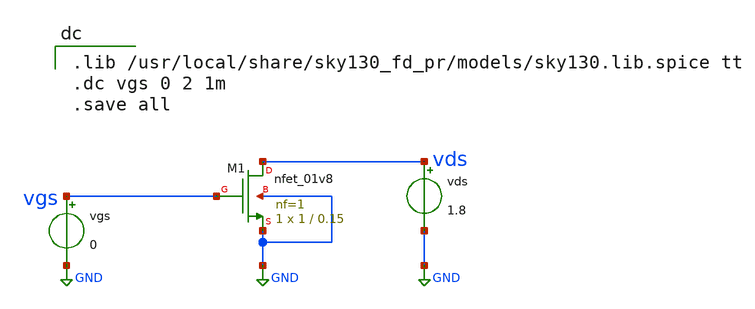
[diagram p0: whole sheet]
** sch_path: files/mos_characteristics/nmos/nmos.sch
**.subckt nmos
XM1 vds vgs GND GND sky130_fd_pr__nfet_01v8 L=0.15 W=1 nf=1 ad='int((1 + 1)/2) * 1 / 1 * 0.29' as='int((1 + 2)/2) * 1 / 1 * 0.29'
+ pd='2*int((1 + 1)/2) * (1 / 1 + 0.29)' ps='2*int((1 + 2)/2) * (1 / 1 + 0.29)' nrd='0.29 / 1 ' nrs='0.29 / 1 '
+ sa=0 sb=0 sd=0 mult=1 m=1
vgs vgs GND 0
vds vds GND 1.8
**** begin user architecture code

.lib /usr/local/share/sky130_fd_pr/models/sky130.lib.spice tt
.dc vgs 0 2 1m
.save all

**** end user architecture code
**.ends
.GLOBAL GND
.end
